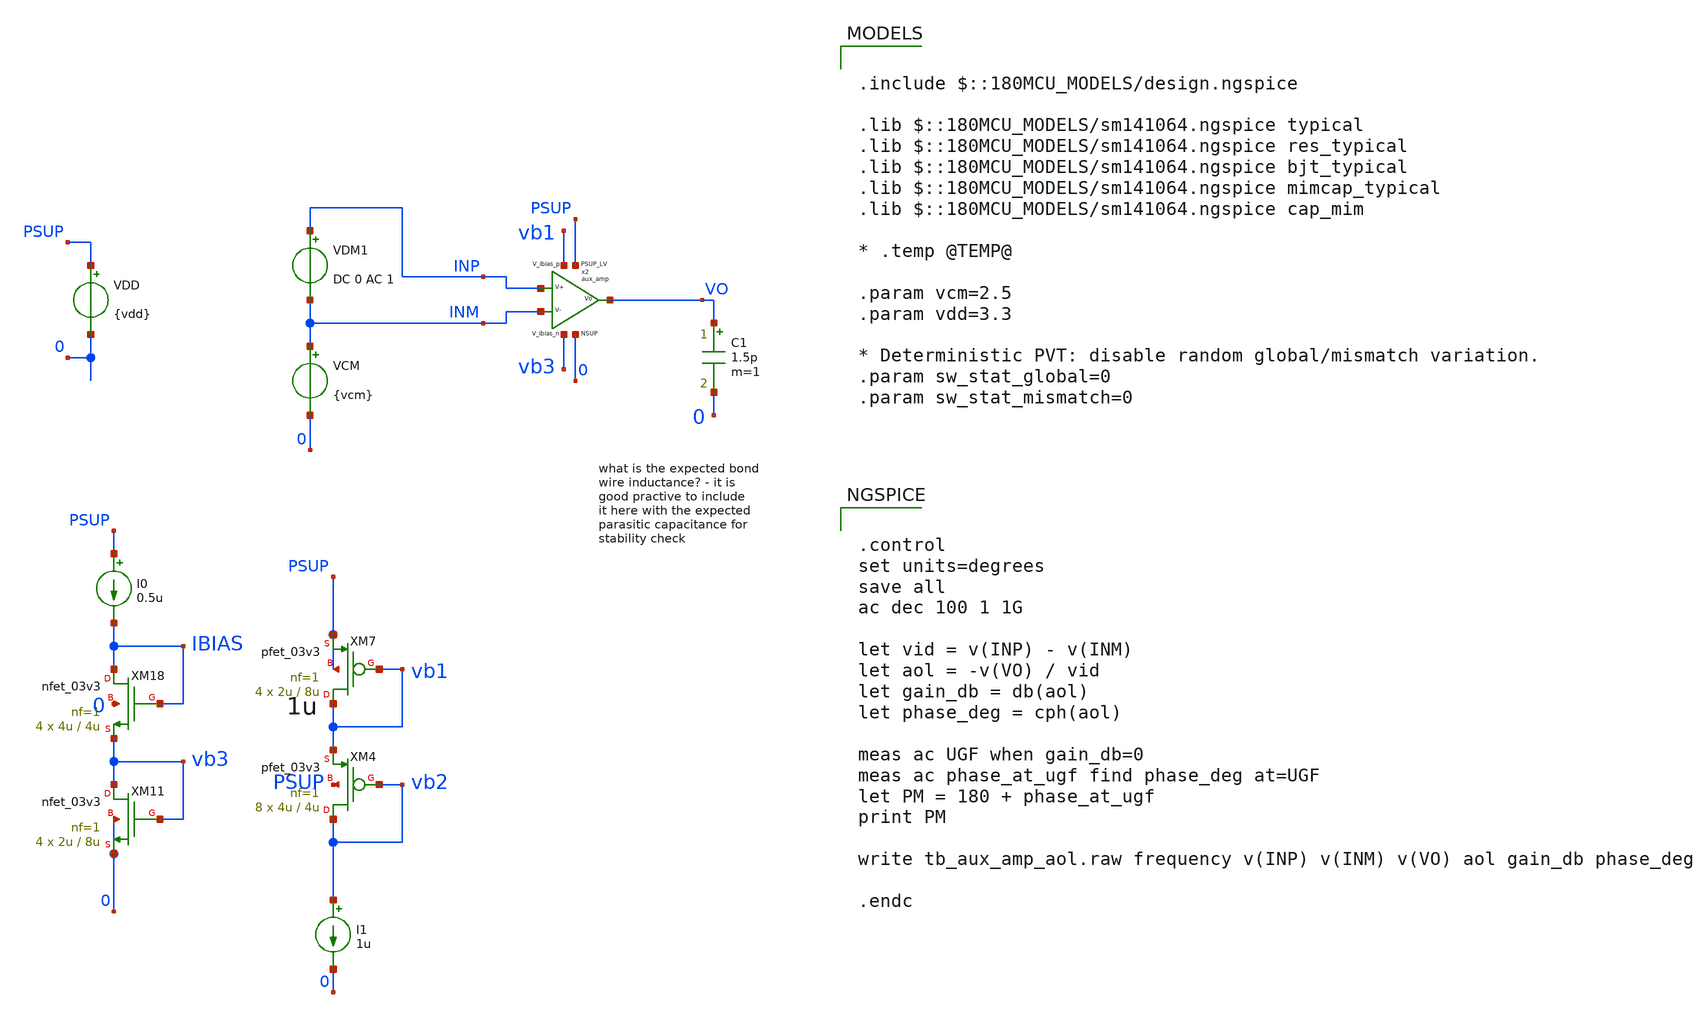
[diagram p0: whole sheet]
** sch_path: xschem/blocks/aux_amp/tb_aux_amp_aol.sch
**.subckt tb_aux_amp_aol
VDD PSUP 0 {vdd}
VCM INM 0 {vcm}
VDM1 INP INM DC 0 AC 1
C1 VO 0 1.5p m=1
XM11 vb3 vb3 0 0 nfet_03v3 L=8u W=2u nf=1 ad='int((nf+1)/2) * W/nf * 0.18u' as='int((nf+2)/2) * W/nf * 0.18u'
+ pd='2*int((nf+1)/2) * (W/nf + 0.18u)' ps='2*int((nf+2)/2) * (W/nf + 0.18u)' nrd='0.18u / W' nrs='0.18u / W'
+ sa=0 sb=0 sd=0 m=4
XM18 IBIAS IBIAS vb3 0 nfet_03v3 L=4u W=4u nf=1 ad='int((nf+1)/2) * W/nf * 0.18u' as='int((nf+2)/2) * W/nf * 0.18u'
+ pd='2*int((nf+1)/2) * (W/nf + 0.18u)' ps='2*int((nf+2)/2) * (W/nf + 0.18u)' nrd='0.18u / W' nrs='0.18u / W'
+ sa=0 sb=0 sd=0 m=4
I0 PSUP IBIAS 0.5u
XM7 vb1 vb1 PSUP PSUP pfet_03v3 L=8u W=2u nf=1 ad='int((nf+1)/2) * W/nf * 0.18u' as='int((nf+2)/2) * W/nf * 0.18u'
+ pd='2*int((nf+1)/2) * (W/nf + 0.18u)' ps='2*int((nf+2)/2) * (W/nf + 0.18u)' nrd='0.18u / W' nrs='0.18u / W'
+ sa=0 sb=0 sd=0 m=4
XM4 vb2 vb2 vb1 PSUP pfet_03v3 L=4u W=4u nf=1 ad='int((nf+1)/2) * W/nf * 0.18u' as='int((nf+2)/2) * W/nf * 0.18u'
+ pd='2*int((nf+1)/2) * (W/nf + 0.18u)' ps='2*int((nf+2)/2) * (W/nf + 0.18u)' nrd='0.18u / W' nrs='0.18u / W'
+ sa=0 sb=0 sd=0 m=8
I1 vb2 0 1u
x2 PSUP VO INP INM vb3 0 vb1 aux_amp
**** begin user architecture code

.include $::180MCU_MODELS/design.ngspice

.lib $::180MCU_MODELS/sm141064.ngspice typical
.lib $::180MCU_MODELS/sm141064.ngspice res_typical
.lib $::180MCU_MODELS/sm141064.ngspice bjt_typical
.lib $::180MCU_MODELS/sm141064.ngspice mimcap_typical
.lib $::180MCU_MODELS/sm141064.ngspice cap_mim

* .temp @TEMP@

.param vcm=2.5
.param vdd=3.3

* Deterministic PVT: disable random global/mismatch variation.
.param sw_stat_global=0
.param sw_stat_mismatch=0



.control
set units=degrees
save all
ac dec 100 1 1G

let vid = v(INP) - v(INM)
let aol = -v(VO) / vid
let gain_db = db(aol)
let phase_deg = cph(aol)

meas ac UGF when gain_db=0
meas ac phase_at_ugf find phase_deg at=UGF
let PM = 180 + phase_at_ugf
print PM

write tb_aux_amp_aol.raw frequency v(INP) v(INM) v(VO) aol gain_db phase_deg

.endc


**** end user architecture code
**.ends

* expanding   symbol:  blocks/aux_amp/aux_amp.sym # of pins=7
** sym_path: xschem/blocks/aux_amp/aux_amp.sym
** sch_path: xschem/blocks/aux_amp/aux_amp.sch
.subckt aux_amp PSUP_LV Vo V+ V- V_ibias_n NSUP V_ibias_p
*.ipin PSUP_LV
*.ipin NSUP
*.ipin V+
*.ipin V-
*.ipin V_ibias_n
*.ipin V_ibias_p
*.opin Vo
XM9 AA1 AA1 PSUP_LV PSUP_LV pfet_03v3 L=0.4u W=16u nf=1 ad='int((nf+1)/2) * W/nf * 0.18u' as='int((nf+2)/2) * W/nf * 0.18u'
+ pd='2*int((nf+1)/2) * (W/nf + 0.18u)' ps='2*int((nf+2)/2) * (W/nf + 0.18u)' nrd='0.18u / W' nrs='0.18u / W'
+ sa=0 sb=0 sd=0 m=1
XM10 Vo AA1 PSUP_LV PSUP_LV pfet_03v3 L=0.4u W=16u nf=1 ad='int((nf+1)/2) * W/nf * 0.18u' as='int((nf+2)/2) * W/nf * 0.18u'
+ pd='2*int((nf+1)/2) * (W/nf + 0.18u)' ps='2*int((nf+2)/2) * (W/nf + 0.18u)' nrd='0.18u / W' nrs='0.18u / W'
+ sa=0 sb=0 sd=0 m=1
XM11 Vo V+ AA2 NSUP nfet_03v3 L=0.5u W=100u nf=1 ad='int((nf+1)/2) * W/nf * 0.18u' as='int((nf+2)/2) * W/nf * 0.18u'
+ pd='2*int((nf+1)/2) * (W/nf + 0.18u)' ps='2*int((nf+2)/2) * (W/nf + 0.18u)' nrd='0.18u / W' nrs='0.18u / W'
+ sa=0 sb=0 sd=0 m=1
XM12 AA1 V- AA2 NSUP nfet_03v3 L=0.5u W=100u nf=1 ad='int((nf+1)/2) * W/nf * 0.18u' as='int((nf+2)/2) * W/nf * 0.18u'
+ pd='2*int((nf+1)/2) * (W/nf + 0.18u)' ps='2*int((nf+2)/2) * (W/nf + 0.18u)' nrd='0.18u / W' nrs='0.18u / W'
+ sa=0 sb=0 sd=0 m=1
XM1 net1 V_ibias_n NSUP NSUP nfet_03v3 L=8u W=2u nf=1 ad='int((nf+1)/2) * W/nf * 0.18u' as='int((nf+2)/2) * W/nf * 0.18u'
+ pd='2*int((nf+1)/2) * (W/nf + 0.18u)' ps='2*int((nf+2)/2) * (W/nf + 0.18u)' nrd='0.18u / W' nrs='0.18u / W'
+ sa=0 sb=0 sd=0 m=70
Vmeas AA2 net1 0
.save i(vmeas)
* noconn V_ibias_p
.ends

.end
